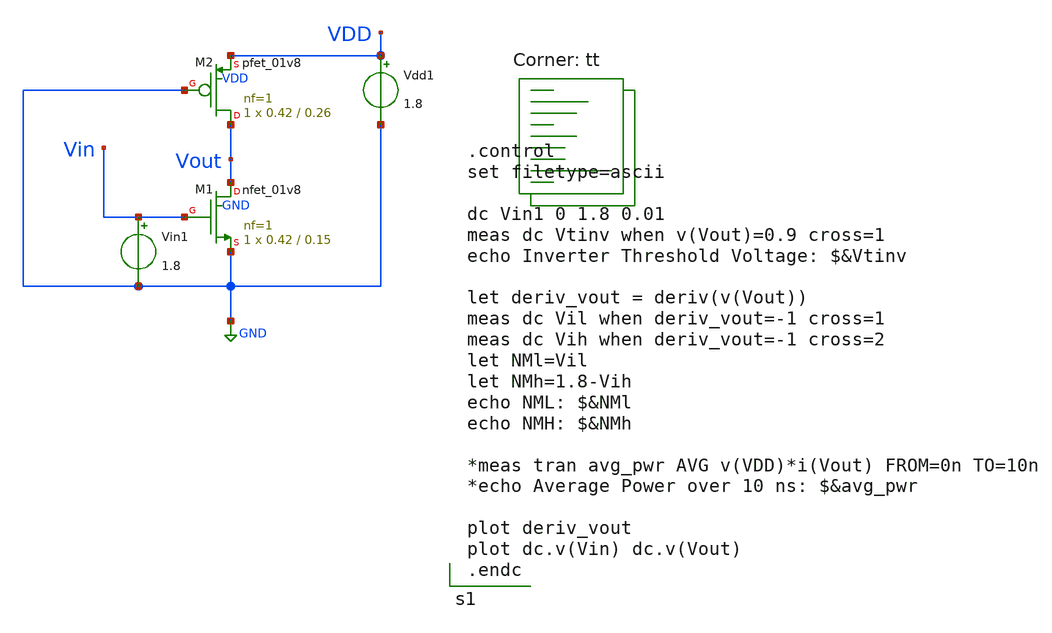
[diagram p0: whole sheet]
** sch_path: tut2/expt1/expt1.sch
**.subckt expt1
XM1 Vout Vin GND GND sky130_fd_pr__nfet_01v8 L=0.15 W=0.42 nf=1 ad='int((nf+1)/2) * W/nf * 0.29' as='int((nf+2)/2) * W/nf * 0.29'
+ pd='2*int((nf+1)/2) * (W/nf + 0.29)' ps='2*int((nf+2)/2) * (W/nf + 0.29)' nrd='0.29 / W' nrs='0.29 / W'
+ sa=0 sb=0 sd=0 mult=1 m=1
Vin1 Vin GND 1.8
XM2 Vout GND VDD VDD sky130_fd_pr__pfet_01v8 L=0.26 W=0.42 nf=1 ad='int((nf+1)/2) * W/nf * 0.29' as='int((nf+2)/2) * W/nf * 0.29'
+ pd='2*int((nf+1)/2) * (W/nf + 0.29)' ps='2*int((nf+2)/2) * (W/nf + 0.29)' nrd='0.29 / W' nrs='0.29 / W'
+ sa=0 sb=0 sd=0 mult=1 m=1
Vdd1 VDD GND 1.8
**** begin user architecture code
.lib $::SKYWATER_MODELS/sky130.lib.spice tt

.control
set filetype=ascii

dc Vin1 0 1.8 0.01
meas dc Vtinv when v(Vout)=0.9 cross=1
echo Inverter Threshold Voltage: $&Vtinv

let deriv_vout = deriv(v(Vout))
meas dc Vil when deriv_vout=-1 cross=1
meas dc Vih when deriv_vout=-1 cross=2
let NMl=Vil
let NMh=1.8-Vih
echo NML: $&NMl
echo NMH: $&NMh

*meas tran avg_pwr AVG v(VDD)*i(Vout) FROM=0n TO=10n
*echo Average Power over 10 ns: $&avg_pwr

plot deriv_vout
plot dc.v(Vin) dc.v(Vout)
.endc

**** end user architecture code
**.ends
.GLOBAL GND
.end
